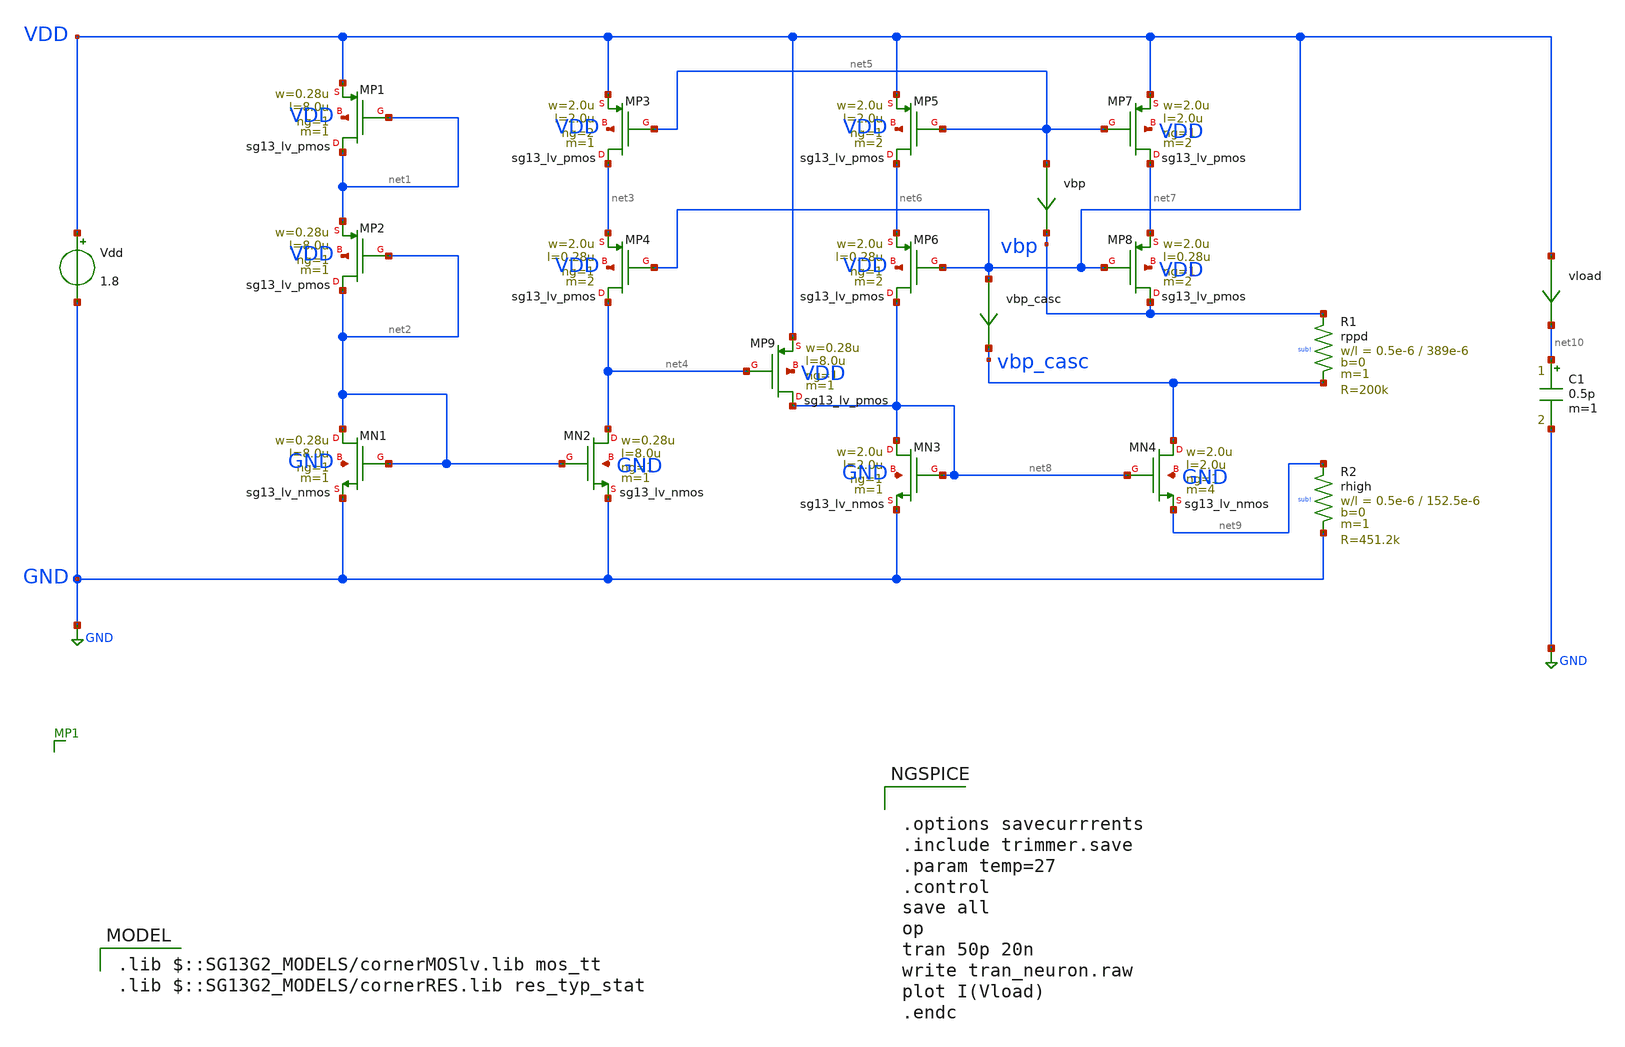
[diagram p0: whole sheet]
** sch_path: blocks/composite/dpi_adexp_neuron/design_data/xschem/trimmer.sch
* Copyright 2023 IHP PDK Authors
**.subckt trimmer
XMP1 net1 net1 VDD VDD sg13_lv_pmos w=0.28u l=8.0u ng=1 m=1 mm_ok=1
XMP2 net2 net2 net1 VDD sg13_lv_pmos w=0.28u l=8.0u ng=1 m=1 mm_ok=1
XMN2 net4 net2 GND GND sg13_lv_nmos w=0.28u l=8.0u ng=1 m=1 mm_ok=1
XMN1 net2 net2 GND GND sg13_lv_nmos w=0.28u l=8.0u ng=1 m=1 mm_ok=1
XMP3 net3 net5 VDD VDD sg13_lv_pmos w=2.0u l=2.0u ng=2 m=1 mm_ok=1
XMP4 net4 VDD net3 VDD sg13_lv_pmos w=2.0u l=0.28u ng=1 m=2 mm_ok=1
XMP5 net6 net5 VDD VDD sg13_lv_pmos w=2.0u l=2.0u ng=1 m=2 mm_ok=1
XMP6 net8 VDD net6 VDD sg13_lv_pmos w=2.0u l=0.28u ng=1 m=2 mm_ok=1
XMP7 net7 net5 VDD VDD sg13_lv_pmos w=2.0u l=2.0u ng=1 m=2 mm_ok=1
XMP8 vbp VDD net7 VDD sg13_lv_pmos w=2.0u l=0.28u ng=1 m=2 mm_ok=1
XMP9 net8 net4 VDD VDD sg13_lv_pmos w=0.28u l=8.0u ng=1 m=1 mm_ok=1
XMN3 net8 net8 GND GND sg13_lv_nmos w=2.0u l=2.0u ng=1 m=1 mm_ok=1
XMN4 vbp_casc net8 net9 GND sg13_lv_nmos w=2.0u l=2.0u ng=1 m=4 mm_ok=1
XR1 vbp vbp_casc sub! rppd w=0.5e-6 l=389e-6 m=1 b=0 mm_ok=1
XR2 net9 GND sub! rhigh w=0.5e-6 l=152.5e-6 m=1 b=0 mm_ok=1
vbp net5 vbp 0
.save i(vbp)
vbp_casc VDD vbp_casc 0
.save i(vbp_casc)
Vdd VDD GND 1.8
vload VDD net10 0
.save i(vload)
C1 net10 GND 0.5p m=1
**** begin user architecture code


.options savecurrrents
.include trimmer.save
.param temp=27
.control
save all
op
tran 50p 20n
write tran_neuron.raw
plot I(Vload)
.endc


 .lib $::SG13G2_MODELS/cornerMOSlv.lib mos_tt
.lib $::SG13G2_MODELS/cornerRES.lib res_typ_stat

**** end user architecture code
**.ends
.GLOBAL GND
.end
